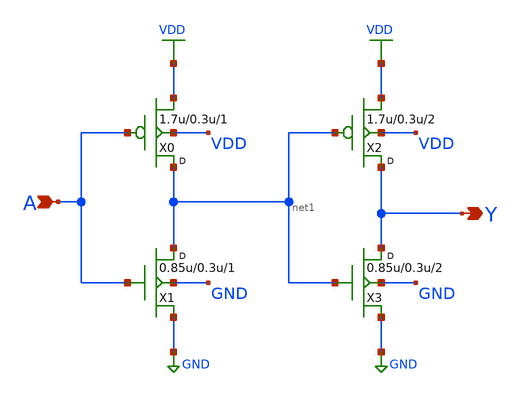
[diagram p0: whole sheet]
** sch_path: gf180mcu_osu_sc_gp12t3v3/cells/buf/gf180mcu_osu_sc_gp12t3v3__buf_2.sch
**.subckt gf180mcu_osu_sc_gp12t3v3__buf_2 A Y
*.ipin A
*.opin Y
X0 net1 A VDD VDD pfet_03p3 w=1.7u l=0.3u m=1
X1 net1 A GND GND nfet_03p3 w=0.85u l=0.3u m=1
X2 Y net1 VDD VDD pfet_03p3 w=1.7u l=0.3u m=2
X3 Y net1 GND GND nfet_03p3 w=0.85u l=0.3u m=2
**.ends
.GLOBAL VDD
.GLOBAL GND
.end
